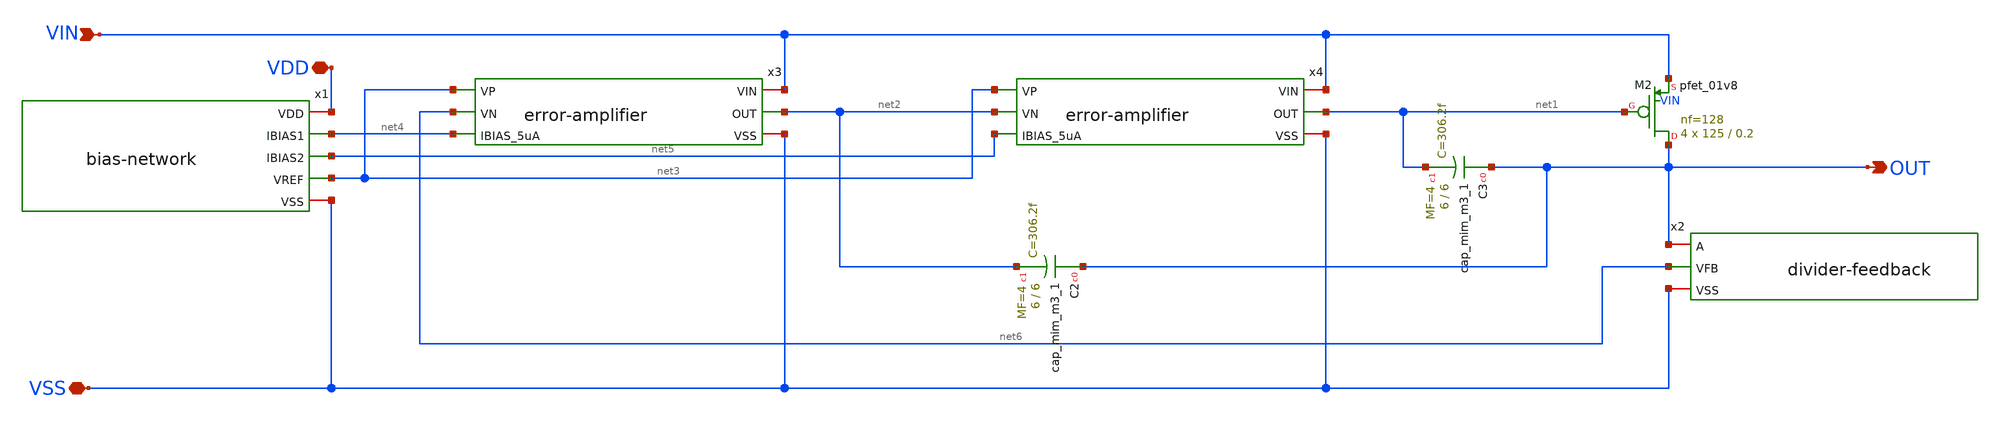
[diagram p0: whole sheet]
** sch_path: xschem/ldo_andriansyah/schematics/ldo-top.sch
**.subckt ldo-top VIN VSS OUT VDD
*.ipin VIN
*.iopin VSS
*.opin OUT
*.iopin VDD
XC2 OUT net2 sky130_fd_pr__cap_mim_m3_1 W=6 L=6 MF=4 m=4
XC3 OUT net1 sky130_fd_pr__cap_mim_m3_1 W=6 L=6 MF=4 m=4
x3 VIN net3 net6 net4 net2 VSS error-amplifier
XM2 OUT net1 VIN VIN sky130_fd_pr__pfet_01v8 L=0.2 W=125 nf=128 ad='int((nf+1)/2) * W/nf * 0.29' as='int((nf+2)/2) * W/nf * 0.29'
+ pd='2*int((nf+1)/2) * (W/nf + 0.29)' ps='2*int((nf+2)/2) * (W/nf + 0.29)' nrd='0.29 / W' nrs='0.29 / W'
+ sa=0 sb=0 sd=0 mult=4 m=4
x4 VIN net3 net2 net5 net1 VSS error-amplifier
x1 VDD net4 net5 net3 VSS bias-network
x2 OUT net6 VSS divider-feedback
**.ends

* expanding   symbol:
*+  /foss/designs/2026/tt_sky26b_ldo_andriansyah/xschem/error-amplifier/error-amplifier.sym # of pins=6
** sym_path: xschem/error-amplifier/error-amplifier.sym
** sch_path: xschem/error-amplifier/error-amplifier.sch
.subckt error-amplifier VIN VP VN IBIAS_5uA OUT VSS
*.ipin IBIAS_5uA
*.ipin VN
*.ipin VP
*.iopin VIN
*.iopin VSS
*.opin OUT
XM1 net2 net2 VSS VSS sky130_fd_pr__nfet_01v8 L=0.6 W=4.2 nf=4 ad='int((nf+1)/2) * W/nf * 0.29' as='int((nf+2)/2) * W/nf * 0.29'
+ pd='2*int((nf+1)/2) * (W/nf + 0.29)' ps='2*int((nf+2)/2) * (W/nf + 0.29)' nrd='0.29 / W' nrs='0.29 / W'
+ sa=0 sb=0 sd=0 mult=1 m=1
XM2 OUT net2 VSS VSS sky130_fd_pr__nfet_01v8 L=0.6 W=4.2 nf=4 ad='int((nf+1)/2) * W/nf * 0.29' as='int((nf+2)/2) * W/nf * 0.29'
+ pd='2*int((nf+1)/2) * (W/nf + 0.29)' ps='2*int((nf+2)/2) * (W/nf + 0.29)' nrd='0.29 / W' nrs='0.29 / W'
+ sa=0 sb=0 sd=0 mult=1 m=1
XM3 net2 VN net1 VIN sky130_fd_pr__pfet_01v8 L=0.6 W=28 nf=4 ad='int((nf+1)/2) * W/nf * 0.29' as='int((nf+2)/2) * W/nf * 0.29'
+ pd='2*int((nf+1)/2) * (W/nf + 0.29)' ps='2*int((nf+2)/2) * (W/nf + 0.29)' nrd='0.29 / W' nrs='0.29 / W'
+ sa=0 sb=0 sd=0 mult=1 m=1
XM4 OUT VP net1 VIN sky130_fd_pr__pfet_01v8 L=0.6 W=28 nf=4 ad='int((nf+1)/2) * W/nf * 0.29' as='int((nf+2)/2) * W/nf * 0.29'
+ pd='2*int((nf+1)/2) * (W/nf + 0.29)' ps='2*int((nf+2)/2) * (W/nf + 0.29)' nrd='0.29 / W' nrs='0.29 / W'
+ sa=0 sb=0 sd=0 mult=1 m=1
XM5 net1 IBIAS_5uA VIN VIN sky130_fd_pr__pfet_01v8 L=0.6 W=6.6 nf=4 ad='int((nf+1)/2) * W/nf * 0.29'
+ as='int((nf+2)/2) * W/nf * 0.29' pd='2*int((nf+1)/2) * (W/nf + 0.29)' ps='2*int((nf+2)/2) * (W/nf + 0.29)'
+ nrd='0.29 / W' nrs='0.29 / W' sa=0 sb=0 sd=0 mult=1 m=1
XM6 IBIAS_5uA IBIAS_5uA VIN VIN sky130_fd_pr__pfet_01v8 L=0.6 W=6.6 nf=4 ad='int((nf+1)/2) * W/nf * 0.29'
+ as='int((nf+2)/2) * W/nf * 0.29' pd='2*int((nf+1)/2) * (W/nf + 0.29)' ps='2*int((nf+2)/2) * (W/nf + 0.29)'
+ nrd='0.29 / W' nrs='0.29 / W' sa=0 sb=0 sd=0 mult=1 m=1
.ends


* expanding   symbol:
*+  /foss/designs/2026/tt_sky26b_ldo_andriansyah/xschem/bias-net/schematics/bias-network.sym # of pins=5
** sym_path: xschem/bias-net/schematics/bias-network.sym
** sch_path: xschem/bias-net/schematics/bias-network.sch
.subckt bias-network VDD IBIAS1 IBIAS2 VREF VSS
*.iopin VDD
*.iopin VSS
*.opin IBIAS1
*.opin IBIAS2
*.opin VREF
XM2 VREF VREF VSS VSS sky130_fd_pr__nfet_01v8 L=2 W=3 nf=4 ad='int((nf+1)/2) * W/nf * 0.29' as='int((nf+2)/2) * W/nf * 0.29'
+ pd='2*int((nf+1)/2) * (W/nf + 0.29)' ps='2*int((nf+2)/2) * (W/nf + 0.29)' nrd='0.29 / W' nrs='0.29 / W'
+ sa=0 sb=0 sd=0 mult=2 m=2
XR1 VREF net1 VSS sky130_fd_pr__res_xhigh_po_0p69 L=6.9 mult=1 m=1
XR2 net2 net1 VSS sky130_fd_pr__res_xhigh_po_0p69 L=6.9 mult=1 m=1
XR3 net2 net3 VSS sky130_fd_pr__res_xhigh_po_0p69 L=6.9 mult=1 m=1
XR4 net4 net3 VSS sky130_fd_pr__res_xhigh_po_0p69 L=6.9 mult=1 m=1
XR5 net4 net5 VSS sky130_fd_pr__res_xhigh_po_0p69 L=6.9 mult=1 m=1
XR6 net9 net10 VSS sky130_fd_pr__res_xhigh_po_0p69 L=6.9 mult=1 m=1
XR7 net9 net8 VSS sky130_fd_pr__res_xhigh_po_0p69 L=6.9 mult=1 m=1
XR8 net7 net8 VSS sky130_fd_pr__res_xhigh_po_0p69 L=6.9 mult=1 m=1
XR9 net7 net6 VSS sky130_fd_pr__res_xhigh_po_0p69 L=6.9 mult=1 m=1
XR10 net5 net6 VSS sky130_fd_pr__res_xhigh_po_0p69 L=6.9 mult=1 m=1
XM1 IBIAS1 VREF VSS VSS sky130_fd_pr__nfet_01v8 L=2 W=3 nf=4 ad='int((nf+1)/2) * W/nf * 0.29' as='int((nf+2)/2) * W/nf * 0.29'
+ pd='2*int((nf+1)/2) * (W/nf + 0.29)' ps='2*int((nf+2)/2) * (W/nf + 0.29)' nrd='0.29 / W' nrs='0.29 / W'
+ sa=0 sb=0 sd=0 mult=2 m=2
XM3 IBIAS2 VREF VSS VSS sky130_fd_pr__nfet_01v8 L=2 W=3 nf=4 ad='int((nf+1)/2) * W/nf * 0.29' as='int((nf+2)/2) * W/nf * 0.29'
+ pd='2*int((nf+1)/2) * (W/nf + 0.29)' ps='2*int((nf+2)/2) * (W/nf + 0.29)' nrd='0.29 / W' nrs='0.29 / W'
+ sa=0 sb=0 sd=0 mult=2 m=2
XR11 net10 net11 VSS sky130_fd_pr__res_xhigh_po_0p69 L=6.9 mult=1 m=1
XR12 net12 net11 VSS sky130_fd_pr__res_xhigh_po_0p69 L=6.9 mult=1 m=1
XR13 net12 net13 VSS sky130_fd_pr__res_xhigh_po_0p69 L=6.9 mult=1 m=1
XR14 net14 net13 VSS sky130_fd_pr__res_xhigh_po_0p69 L=6.9 mult=1 m=1
XR15 net14 net15 VSS sky130_fd_pr__res_xhigh_po_0p69 L=6.9 mult=1 m=1
XR16 net19 VDD VSS sky130_fd_pr__res_xhigh_po_0p69 L=6.9 mult=1 m=1
XR17 net19 net18 VSS sky130_fd_pr__res_xhigh_po_0p69 L=6.9 mult=1 m=1
XR18 net17 net18 VSS sky130_fd_pr__res_xhigh_po_0p69 L=6.9 mult=1 m=1
XR19 net17 net16 VSS sky130_fd_pr__res_xhigh_po_0p69 L=6.9 mult=1 m=1
XR20 net15 net16 VSS sky130_fd_pr__res_xhigh_po_0p69 L=6.9 mult=1 m=1
XR21 VSS VSS VSS sky130_fd_pr__res_xhigh_po_0p69 L=6.9 mult=1 m=1
XR22 VSS VSS VSS sky130_fd_pr__res_xhigh_po_0p69 L=6.9 mult=1 m=1
.ends


* expanding   symbol:
*+  /foss/designs/2026/tt_sky26b_ldo_andriansyah/xschem/divider-feedback/schematics/divider-feedback.sym # of pins=3
** sym_path: xschem/divider-feedback/schematics/divider-feedback.sym
** sch_path: xschem/divider-feedback/schematics/divider-feedback.sch
.subckt divider-feedback A VFB VSS
*.iopin VSS
*.iopin A
*.opin VFB
XR2 VFB net1 VSS sky130_fd_pr__res_xhigh_po_0p69 L=6.9 mult=1 m=1
XR3 net1 net2 VSS sky130_fd_pr__res_xhigh_po_0p69 L=6.9 mult=1 m=1
XR4 net2 net3 VSS sky130_fd_pr__res_xhigh_po_0p69 L=6.9 mult=1 m=1
XR5 net3 net4 VSS sky130_fd_pr__res_xhigh_po_0p69 L=6.9 mult=1 m=1
XR6 net4 net5 VSS sky130_fd_pr__res_xhigh_po_0p69 L=6.9 mult=1 m=1
XR7 net5 net6 VSS sky130_fd_pr__res_xhigh_po_0p69 L=6.9 mult=1 m=1
XR8 net6 net7 VSS sky130_fd_pr__res_xhigh_po_0p69 L=6.9 mult=1 m=1
XR9 net7 net8 VSS sky130_fd_pr__res_xhigh_po_0p69 L=6.9 mult=1 m=1
XR10 net8 net9 VSS sky130_fd_pr__res_xhigh_po_0p69 L=6.9 mult=1 m=1
XR11 net9 A VSS sky130_fd_pr__res_xhigh_po_0p69 L=6.9 mult=1 m=1
XR13 VSS net10 VSS sky130_fd_pr__res_xhigh_po_0p69 L=6.9 mult=1 m=1
XR14 net10 net11 VSS sky130_fd_pr__res_xhigh_po_0p69 L=6.9 mult=1 m=1
XR15 net11 net12 VSS sky130_fd_pr__res_xhigh_po_0p69 L=6.9 mult=1 m=1
XR16 net12 net13 VSS sky130_fd_pr__res_xhigh_po_0p69 L=6.9 mult=1 m=1
XR17 net13 net14 VSS sky130_fd_pr__res_xhigh_po_0p69 L=6.9 mult=1 m=1
XR18 net14 net15 VSS sky130_fd_pr__res_xhigh_po_0p69 L=6.9 mult=1 m=1
XR19 net15 net16 VSS sky130_fd_pr__res_xhigh_po_0p69 L=6.9 mult=1 m=1
XR20 net16 net17 VSS sky130_fd_pr__res_xhigh_po_0p69 L=6.9 mult=1 m=1
XR21 net17 net18 VSS sky130_fd_pr__res_xhigh_po_0p69 L=6.9 mult=1 m=1
XR22 net18 VFB VSS sky130_fd_pr__res_xhigh_po_0p69 L=6.9 mult=1 m=1
XR23 VSS VSS VSS sky130_fd_pr__res_xhigh_po_0p69 L=6.9 mult=1 m=1
XR24 VSS VSS VSS sky130_fd_pr__res_xhigh_po_0p69 L=6.9 mult=1 m=1
.ends

.end
